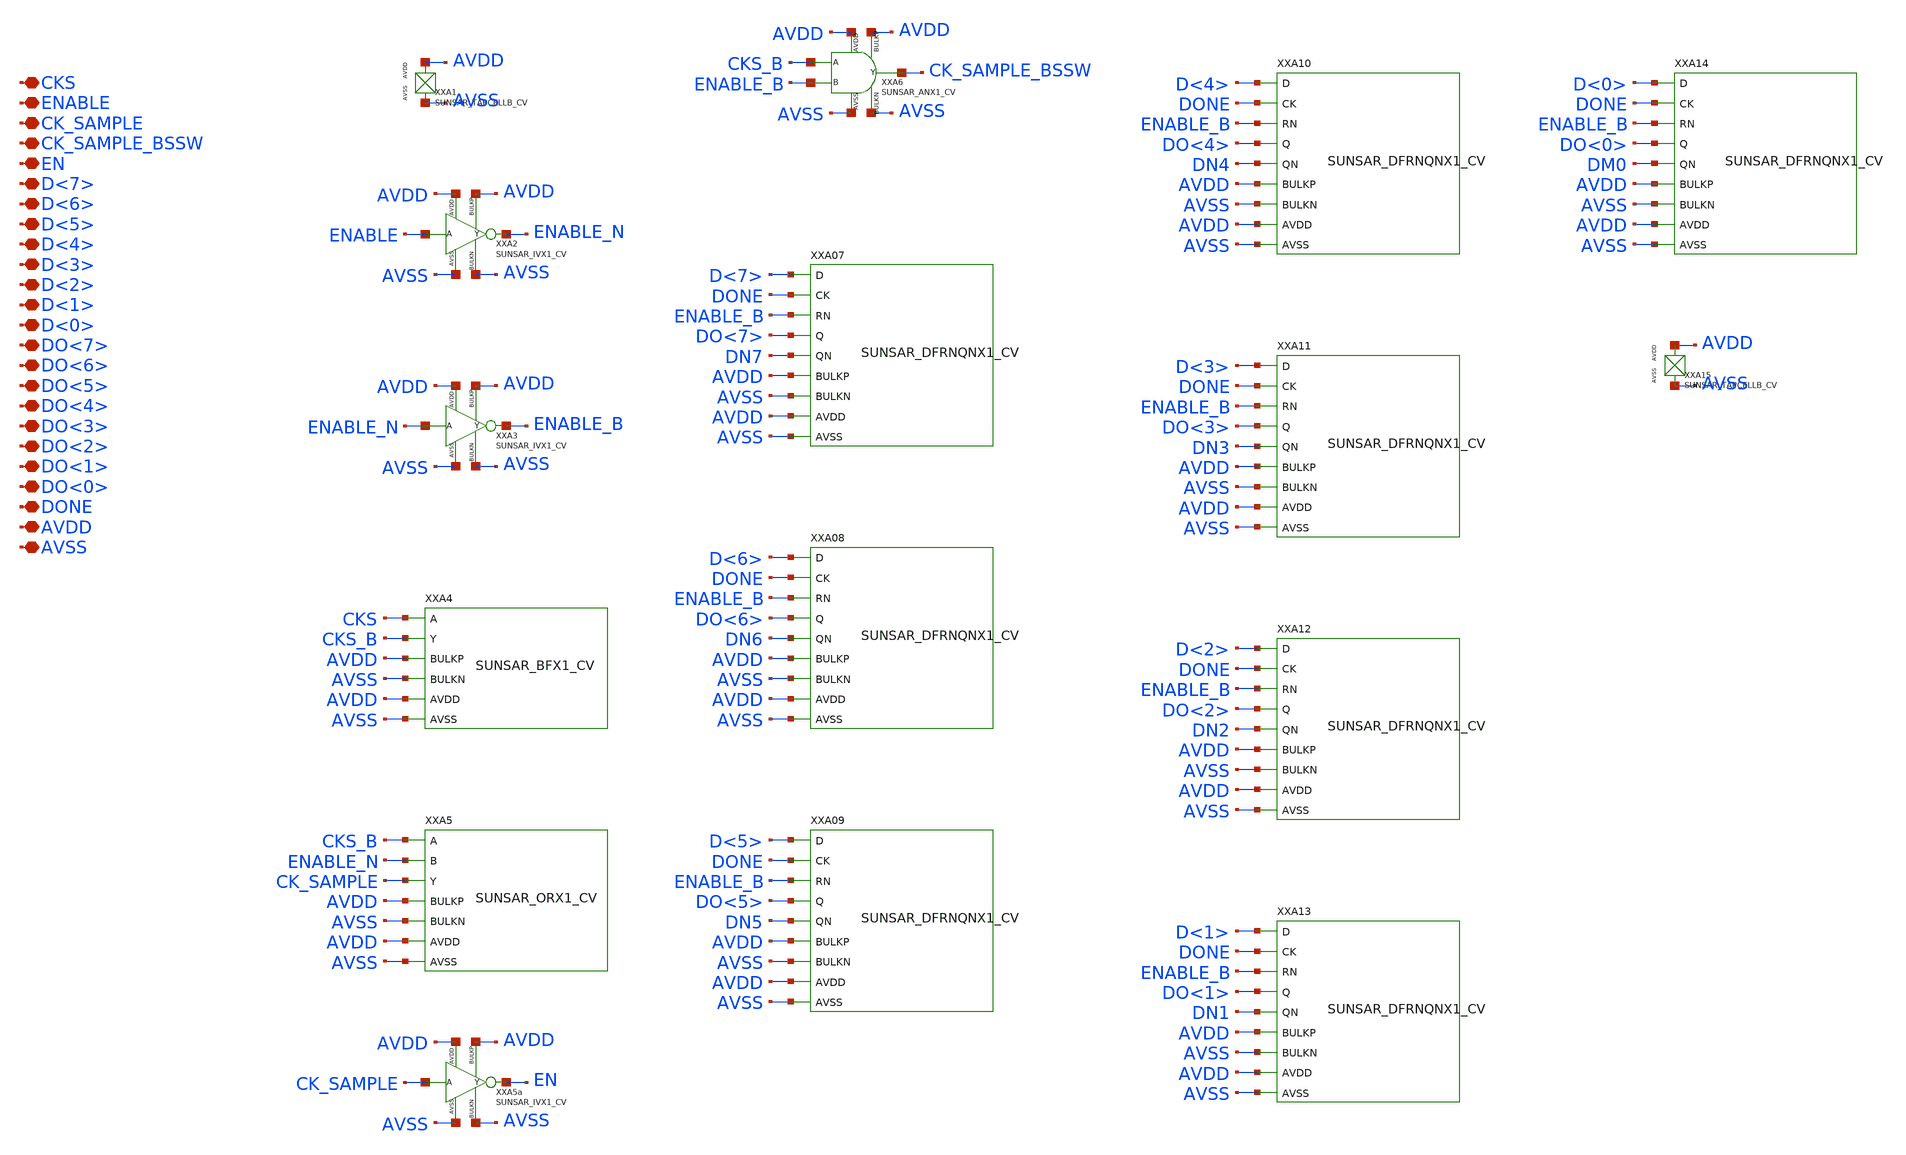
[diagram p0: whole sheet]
** sch_path: design/SUN_SAR9B_SKY130NM/SUNSAR_SARCAPTURE_CV.sch
**.subckt SUNSAR_SARCAPTURE_CV CKS ENABLE CK_SAMPLE CK_SAMPLE_BSSW EN D<7> D<6> D<5> D<4> D<3> D<2>
*+ D<1> D<0> DO<7> DO<6> DO<5> DO<4> DO<3> DO<2> DO<1> DO<0> DONE AVDD AVSS
*.iopin CKS
*.iopin ENABLE
*.iopin CK_SAMPLE
*.iopin CK_SAMPLE_BSSW
*.iopin EN
*.iopin D<7>
*.iopin D<6>
*.iopin D<5>
*.iopin D<4>
*.iopin D<3>
*.iopin D<2>
*.iopin D<1>
*.iopin D<0>
*.iopin DO<7>
*.iopin DO<6>
*.iopin DO<5>
*.iopin DO<4>
*.iopin DO<3>
*.iopin DO<2>
*.iopin DO<1>
*.iopin DO<0>
*.iopin DONE
*.iopin AVDD
*.iopin AVSS
XXA1 AVDD AVSS SUNSAR_TAPCELLB_CV
XXA2 ENABLE ENABLE_N AVDD AVSS AVDD AVSS SUNSAR_IVX1_CV
XXA3 ENABLE_N ENABLE_B AVDD AVSS AVDD AVSS SUNSAR_IVX1_CV
XXA4 CKS CKS_B AVDD AVSS AVDD AVSS SUNSAR_BFX1_CV
XXA5 CKS_B ENABLE_N CK_SAMPLE AVDD AVSS AVDD AVSS SUNSAR_ORX1_CV
XXA5a CK_SAMPLE EN AVDD AVSS AVDD AVSS SUNSAR_IVX1_CV
XXA6 CKS_B ENABLE_B CK_SAMPLE_BSSW AVDD AVSS AVSS AVDD SUNSAR_ANX1_CV
XXA07 D<7> DONE ENABLE_B DO<7> DN7 AVDD AVSS AVDD AVSS SUNSAR_DFRNQNX1_CV
XXA08 D<6> DONE ENABLE_B DO<6> DN6 AVDD AVSS AVDD AVSS SUNSAR_DFRNQNX1_CV
XXA09 D<5> DONE ENABLE_B DO<5> DN5 AVDD AVSS AVDD AVSS SUNSAR_DFRNQNX1_CV
XXA10 D<4> DONE ENABLE_B DO<4> DN4 AVDD AVSS AVDD AVSS SUNSAR_DFRNQNX1_CV
XXA11 D<3> DONE ENABLE_B DO<3> DN3 AVDD AVSS AVDD AVSS SUNSAR_DFRNQNX1_CV
XXA12 D<2> DONE ENABLE_B DO<2> DN2 AVDD AVSS AVDD AVSS SUNSAR_DFRNQNX1_CV
XXA13 D<1> DONE ENABLE_B DO<1> DN1 AVDD AVSS AVDD AVSS SUNSAR_DFRNQNX1_CV
XXA14 D<0> DONE ENABLE_B DO<0> DM0 AVDD AVSS AVDD AVSS SUNSAR_DFRNQNX1_CV
XXA15 AVDD AVSS SUNSAR_TAPCELLB_CV
**.ends
.end
